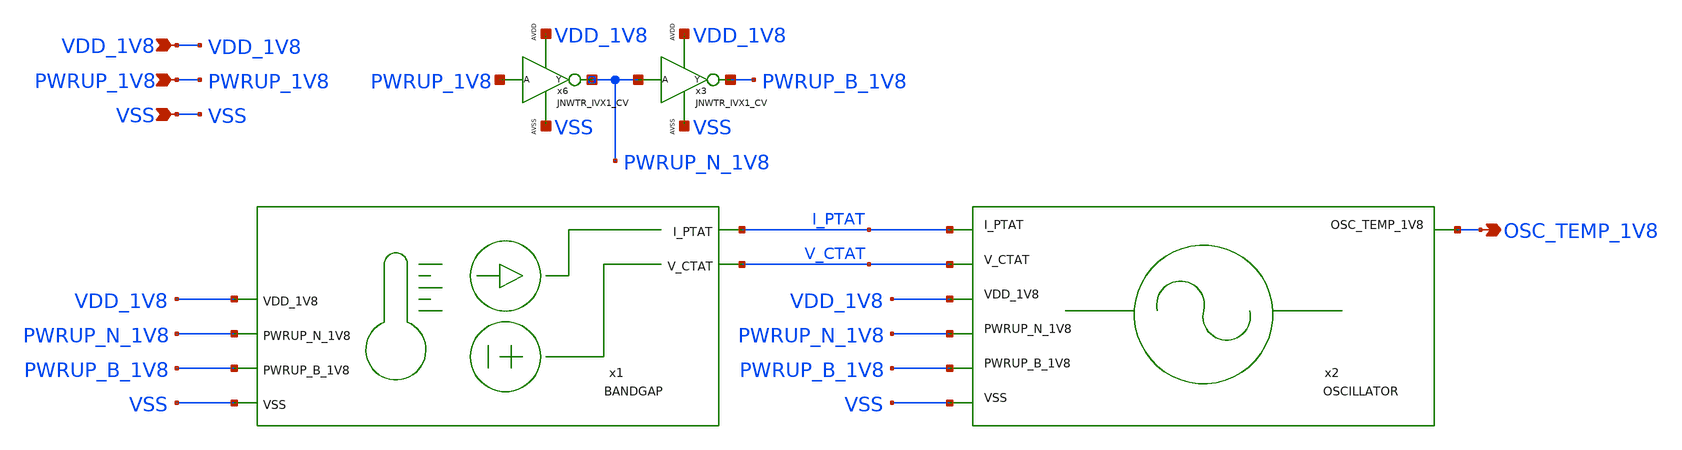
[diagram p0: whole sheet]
** sch_path: design/LELO_GR02_SKY130A/LELO_GR02.sch
**.subckt LELO_GR02 VSS PWRUP_1V8 OSC_TEMP_1V8 VDD_1V8
*.ipin VSS
*.ipin PWRUP_1V8
*.opin OSC_TEMP_1V8
*.ipin VDD_1V8
x1 VDD_1V8 I_PTAT V_CTAT PWRUP_N_1V8 VSS PWRUP_B_1V8 BANDGAP
x2 OSC_TEMP_1V8 VDD_1V8 PWRUP_N_1V8 VSS V_CTAT I_PTAT PWRUP_B_1V8 OSCILLATOR
x6 PWRUP_1V8 PWRUP_N_1V8 VDD_1V8 VSS JNWTR_IVX1_CV
x3 PWRUP_N_1V8 PWRUP_B_1V8 VDD_1V8 VSS JNWTR_IVX1_CV
**.ends
.end
